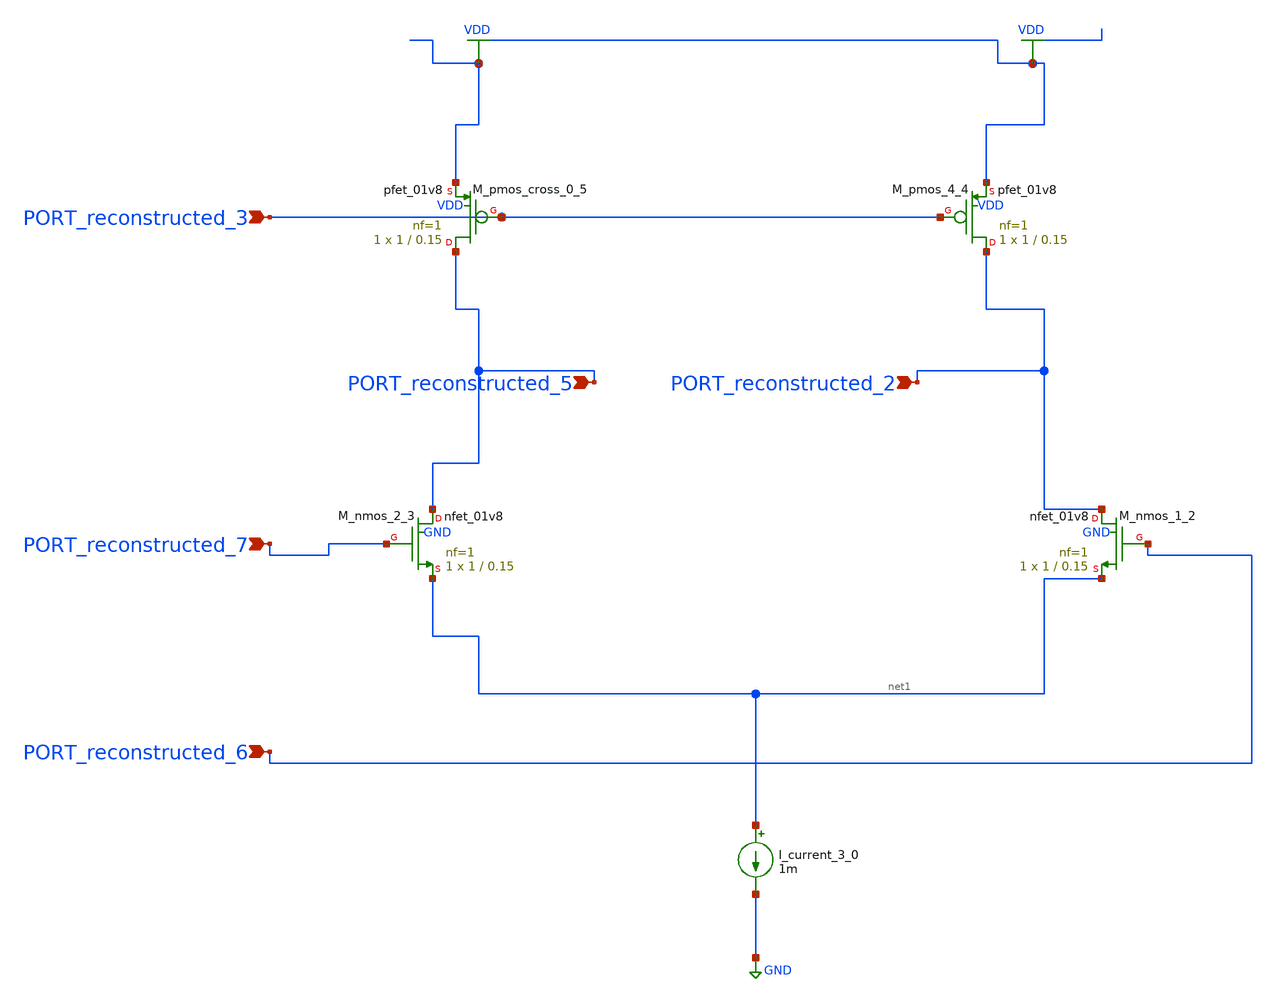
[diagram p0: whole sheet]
** sch_path: schematics/AMSNet/813.sch
**.subckt 813 PORT_reconstructed_6 PORT_reconstructed_5 PORT_reconstructed_2 PORT_reconstructed_3
*+ PORT_reconstructed_7
*.ipin PORT_reconstructed_6
*.ipin PORT_reconstructed_5
*.ipin PORT_reconstructed_2
*.ipin PORT_reconstructed_3
*.ipin PORT_reconstructed_7
I_current_3_0 net1 GND 1m
XM_nmos_1_2 PORT_reconstructed_2 PORT_reconstructed_6 net1 GND sky130_fd_pr__nfet_01v8 L=0.15 W=1 nf=1
+ ad='int((1 + 1)/2) * 1 / 1 * 0.29' as='int((1 + 2)/2) * 1 / 1 * 0.29' pd='2*int((1 + 1)/2) * (1 / 1 + 0.29)'
+ ps='2*int((1 + 2)/2) * (1 / 1 + 0.29)' nrd='0.29 / 1 ' nrs='0.29 / 1 ' sa=0 sb=0 sd=0 mult=1 m=1
XM_nmos_2_3 PORT_reconstructed_5 PORT_reconstructed_7 net1 GND sky130_fd_pr__nfet_01v8 L=0.15 W=1 nf=1
+ ad='int((1 + 1)/2) * 1 / 1 * 0.29' as='int((1 + 2)/2) * 1 / 1 * 0.29' pd='2*int((1 + 1)/2) * (1 / 1 + 0.29)'
+ ps='2*int((1 + 2)/2) * (1 / 1 + 0.29)' nrd='0.29 / 1 ' nrs='0.29 / 1 ' sa=0 sb=0 sd=0 mult=1 m=1
XM_pmos_4_4 PORT_reconstructed_2 PORT_reconstructed_3 VDD VDD sky130_fd_pr__pfet_01v8 L=0.15 W=1 nf=1
+ ad='int((1 + 1)/2) * 1 / 1 * 0.29' as='int((1 + 2)/2) * 1 / 1 * 0.29' pd='2*int((1 + 1)/2) * (1 / 1 + 0.29)'
+ ps='2*int((1 + 2)/2) * (1 / 1 + 0.29)' nrd='0.29 / 1 ' nrs='0.29 / 1 ' sa=0 sb=0 sd=0 mult=1 m=1
XM_pmos_cross_0_5 PORT_reconstructed_5 PORT_reconstructed_3 VDD VDD sky130_fd_pr__pfet_01v8 L=0.15 W=1
+ nf=1 ad='int((1 + 1)/2) * 1 / 1 * 0.29' as='int((1 + 2)/2) * 1 / 1 * 0.29' pd='2*int((1 + 1)/2) * (1 / 1 + 0.29)'
+ ps='2*int((1 + 2)/2) * (1 / 1 + 0.29)' nrd='0.29 / 1 ' nrs='0.29 / 1 ' sa=0 sb=0 sd=0 mult=1 m=1
**.ends
.GLOBAL GND
.GLOBAL VDD
.end
